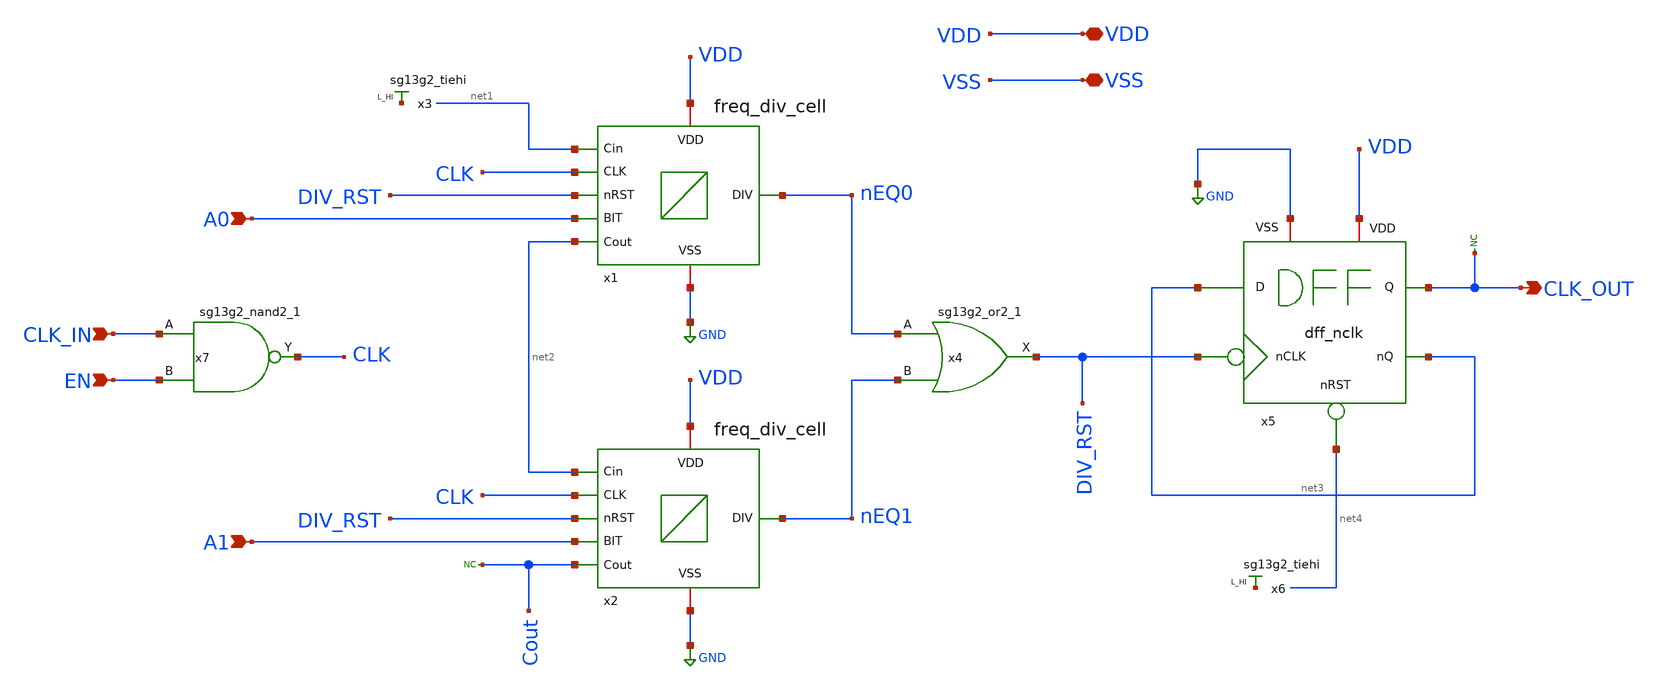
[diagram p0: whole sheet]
** sch_path: Combined Design/design_data/xschem/2-bit_freq_divider.sch
**.subckt 2-bit_freq_divider CLK_IN EN A0 A1 CLK_OUT VSS VDD
*.ipin CLK_IN
*.ipin EN
*.ipin A0
*.ipin A1
*.opin CLK_OUT
*.iopin VSS
*.iopin VDD
x1 VDD GND nEQ0 net1 CLK net2 DIV_RST A0 freq_div_cell
x2 VDD GND nEQ1 net2 CLK Cout DIV_RST A1 freq_div_cell
x3 net5 VDD VSS sg13g2_tiehi
* noconn Cout
x4 DIV_RST nEQ0 nEQ1 VDD VSS sg13g2_or2_1
x5 DIV_RST CLK_OUT net3 net3 net4 VDD GND dff_nclk
x6 net6 VDD VSS sg13g2_tiehi
* noconn CLK_OUT
x7 CLK CLK_IN EN VDD VSS sg13g2_nand2_1
**.ends

* expanding   symbol:  sg13g2_stdcells/sg13g2_or2_1.sym # of pins=3
** sym_path: sg13g2_stdcells/sg13g2_or2_1.sym
** sch_path: sg13g2_stdcells/sg13g2_or2_1.sch
.subckt sg13g2_or2_1 X A B VDD VSS
*.opin X
*.ipin B
*.ipin A
*.iopin VDD
*.iopin VSS
XM1 net1 B VSS VSS sg13_lv_nmos w=550.00n l=130.00n ng=1 m=1 mm_ok=1
XM2 net1 A VSS VSS sg13_lv_nmos w=550.00n l=130.00n ng=1 m=1 mm_ok=1
XM3 X net1 VSS VSS sg13_lv_nmos w=740.00n l=130.00n ng=1 m=1 mm_ok=1
XM4 net2 A VDD VDD sg13_lv_pmos w=840.00n l=130.00n ng=1 m=1 mm_ok=1
XM5 net1 B net2 VDD sg13_lv_pmos w=840.00n l=130.00n ng=1 m=1 mm_ok=1
XM6 X net1 VDD VDD sg13_lv_pmos w=1.12u l=130.00n ng=1 m=1 mm_ok=1
.ends


* expanding   symbol:  sg13g2_stdcells/sg13g2_nand2_1.sym # of pins=3
** sym_path: sg13g2_stdcells/sg13g2_nand2_1.sym
** sch_path: sg13g2_stdcells/sg13g2_nand2_1.sch
.subckt sg13g2_nand2_1 Y A B VDD VSS
*.iopin VDD
*.iopin VSS
*.ipin A
*.ipin B
*.opin Y
XM1 Y A net1 VSS sg13_lv_nmos w=740.00n l=130.00n ng=1 m=1 mm_ok=1
XM2 net1 B VSS VSS sg13_lv_nmos w=740.00n l=130.00n ng=1 m=1 mm_ok=1
XM3 Y A VDD VDD sg13_lv_pmos w=1.12u l=130.00n ng=1 m=1 mm_ok=1
XM4 Y B VDD VDD sg13_lv_pmos w=1.12u l=130.00n ng=1 m=1 mm_ok=1
.ends

.GLOBAL GND
.end
